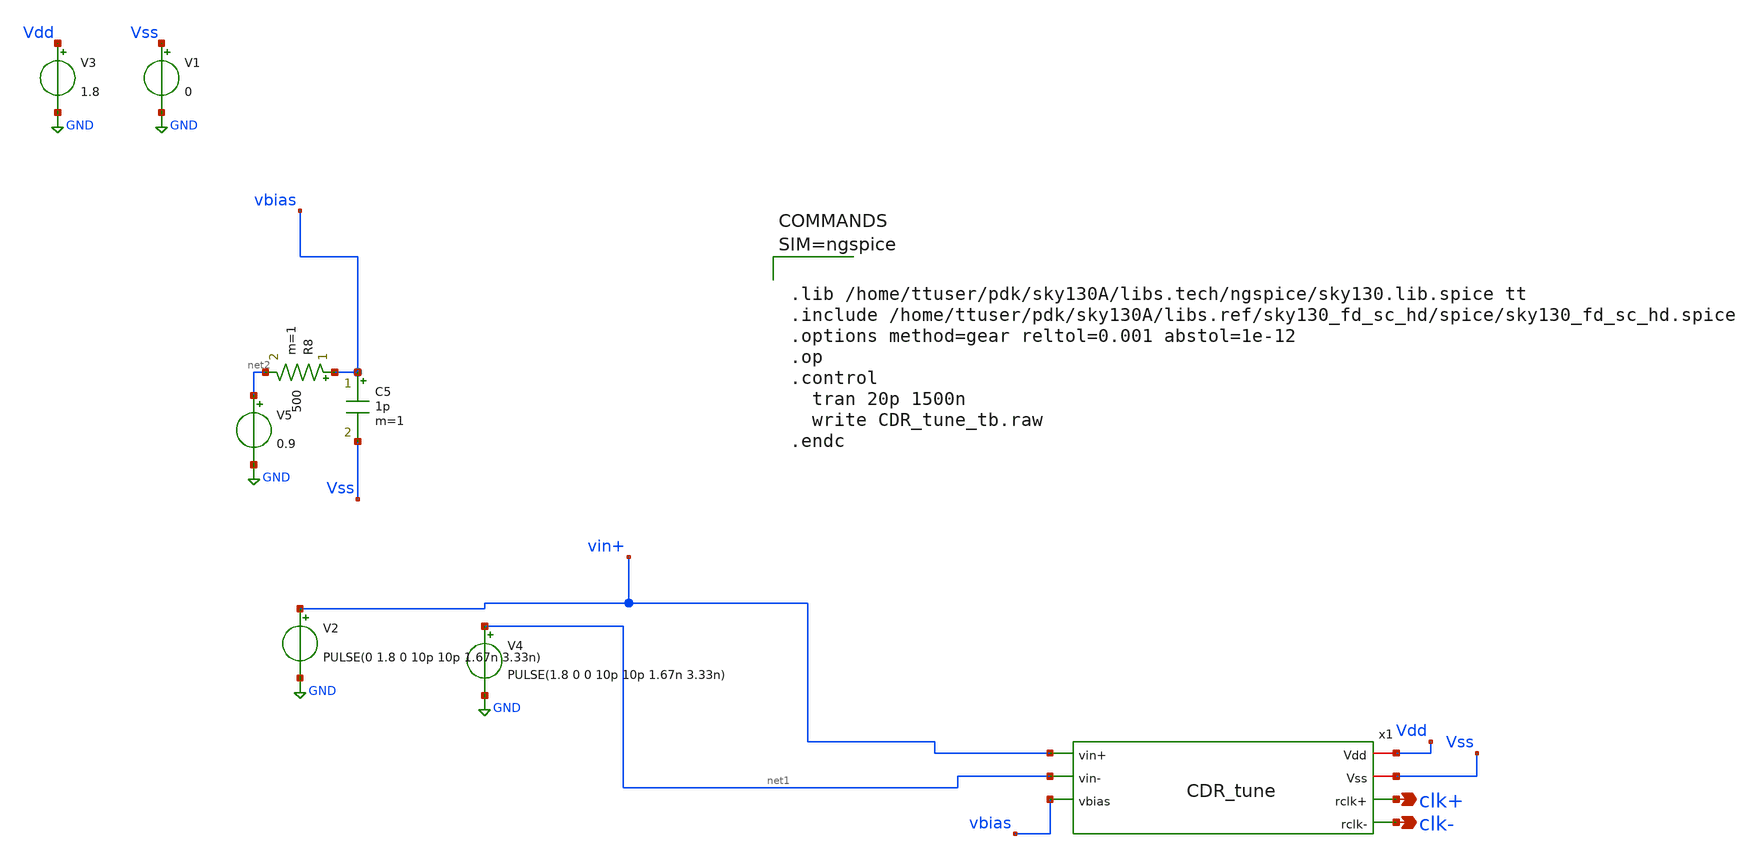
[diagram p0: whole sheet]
** sch_path: xschem/tuning/CDR_tune_tb.sch
**.subckt CDR_tune_tb clk- clk+
*.opin clk-
*.opin clk+
V3 Vdd GND 1.8
V1 Vss GND 0
V2 vin+ GND PULSE(0 1.8 0 10p 10p 1.67n 3.33n)
V4 net1 GND PULSE(1.8 0 0 10p 10p 1.67n 3.33n)
V5 net2 GND 0.9
R8 vbias net2 500 m=1
C5 vbias Vss 1p m=1
x1 Vdd Vss vin+ net1 vbias clk+ clk- CDR_tune
**** begin user architecture code



.lib /home/ttuser/pdk/sky130A/libs.tech/ngspice/sky130.lib.spice tt
.include /home/ttuser/pdk/sky130A/libs.ref/sky130_fd_sc_hd/spice/sky130_fd_sc_hd.spice
.options method=gear reltol=0.001 abstol=1e-12
.op
.control
  tran 20p 1500n
  write CDR_tune_tb.raw
.endc



**** end user architecture code
**.ends
.GLOBAL GND
.end
